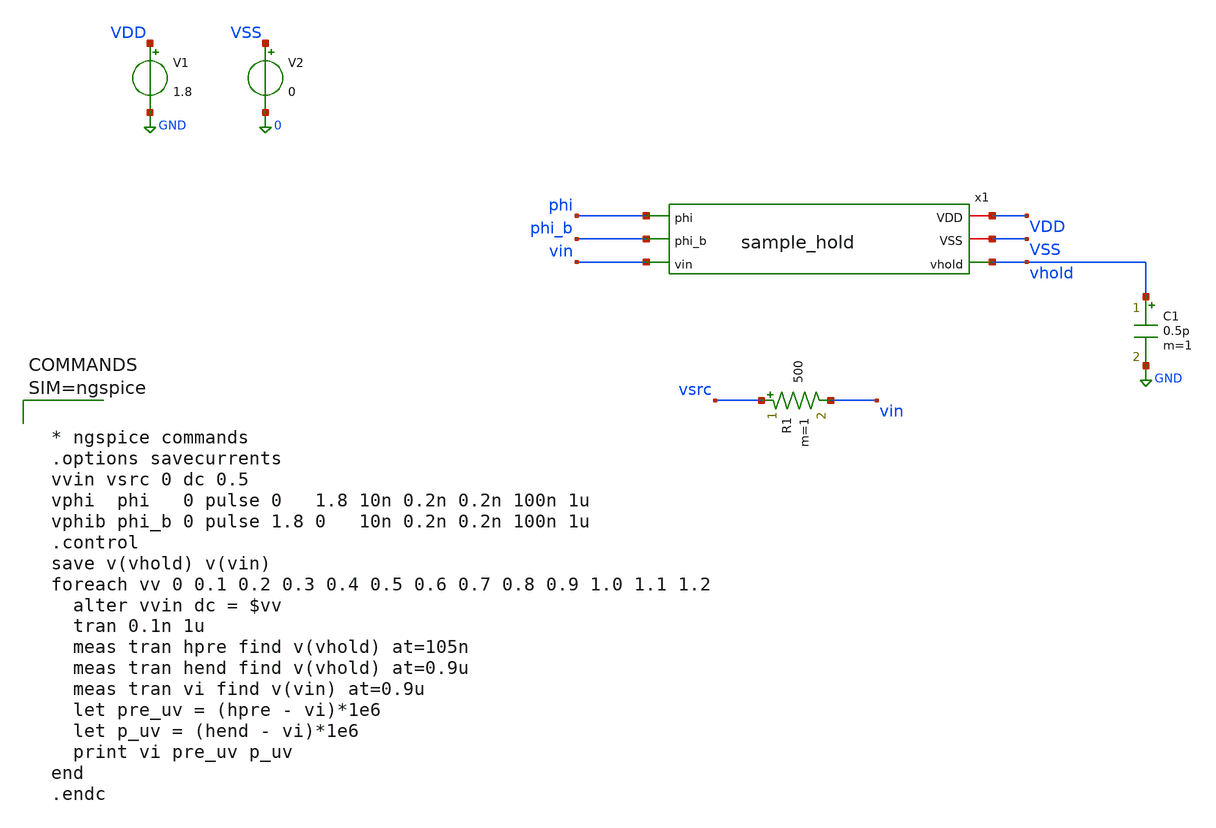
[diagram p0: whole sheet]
** sch_path: xschem/sample_hold_tb.sch
**.subckt sample_hold_tb
V1 VDD GND 1.8
V2 VSS 0 0
x1 phi phi_b VDD VSS vin vhold sample_hold
R1 vsrc vin 500 m=1
C1 vhold GND 0.5p m=1
**** begin user architecture code

** opencircuitdesign pdks install
.lib $::SKYWATER_MODELS/sky130.lib.spice tt




 * ngspice commands
 .options savecurrents
 vvin vsrc 0 dc 0.5
 vphi  phi   0 pulse 0   1.8 10n 0.2n 0.2n 100n 1u
 vphib phi_b 0 pulse 1.8 0   10n 0.2n 0.2n 100n 1u
 .control
 save v(vhold) v(vin)
 foreach vv 0 0.1 0.2 0.3 0.4 0.5 0.6 0.7 0.8 0.9 1.0 1.1 1.2
   alter vvin dc = $vv
   tran 0.1n 1u
   meas tran hpre find v(vhold) at=105n
   meas tran hend find v(vhold) at=0.9u
   meas tran vi find v(vin) at=0.9u
   let pre_uv = (hpre - vi)*1e6
   let p_uv = (hend - vi)*1e6
   print vi pre_uv p_uv
 end
 .endc



**** end user architecture code
**.ends

* expanding   symbol:  sample_hold.sym # of pins=6
** sym_path: xschem/sample_hold.sym
** sch_path: xschem/sample_hold.sch
.subckt sample_hold phi phi_b VDD VSS vin vhold
*.iopin VDD
*.iopin VSS
*.opin vhold
*.ipin phi_b
*.ipin phi
*.ipin vin
XM2 vin phi_b vhold VDD sky130_fd_pr__pfet_01v8 L=0.15 W=8 nf=2 ad='int((2 + 1)/2) * 8 / 2 * 0.29' as='int((2 + 2)/2) * 8 / 2 * 0.29'
+ pd='2*int((2 + 1)/2) * (8 / 2 + 0.29)' ps='2*int((2 + 2)/2) * (8 / 2 + 0.29)' nrd='0.29 / 8 ' nrs='0.29 / 8 '
+ sa=0 sb=0 sd=0 mult=1 m=1
XM4 vhold phi vhold VDD sky130_fd_pr__pfet_01v8 L=0.15 W=4 nf=1 ad='int((1 + 1)/2) * 4 / 1 * 0.29' as='int((1 + 2)/2) * 4 / 1 * 0.29'
+ pd='2*int((1 + 1)/2) * (4 / 1 + 0.29)' ps='2*int((1 + 2)/2) * (4 / 1 + 0.29)' nrd='0.29 / 4 ' nrs='0.29 / 4 '
+ sa=0 sb=0 sd=0 mult=1 m=1
XM1 vin phi vhold VSS sky130_fd_pr__nfet_01v8 L=0.15 W=4 nf=2 ad='int((2 + 1)/2) * 4 / 2 * 0.29' as='int((2 + 2)/2) * 4 / 2 * 0.29'
+ pd='2*int((2 + 1)/2) * (4 / 2 + 0.29)' ps='2*int((2 + 2)/2) * (4 / 2 + 0.29)' nrd='0.29 / 4 ' nrs='0.29 / 4 '
+ sa=0 sb=0 sd=0 mult=1 m=1
XM3 vhold phi_b vhold VSS sky130_fd_pr__nfet_01v8 L=0.15 W=2 nf=1 ad='int((1 + 1)/2) * 2 / 1 * 0.29'
+ as='int((1 + 2)/2) * 2 / 1 * 0.29' pd='2*int((1 + 1)/2) * (2 / 1 + 0.29)' ps='2*int((1 + 2)/2) * (2 / 1 + 0.29)'
+ nrd='0.29 / 2 ' nrs='0.29 / 2 ' sa=0 sb=0 sd=0 mult=1 m=1
XC1 vhold VSS sky130_fd_pr__cap_mim_m3_1 W=22 L=22 MF=2 m=2
.ends

.GLOBAL GND
.end
